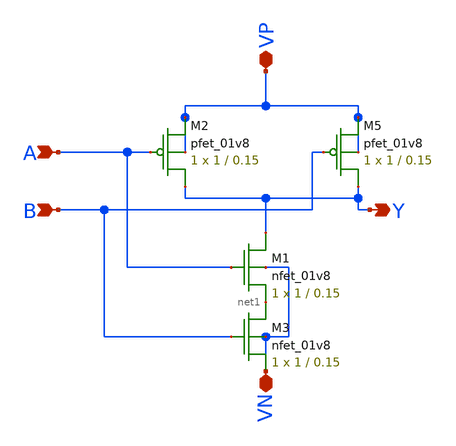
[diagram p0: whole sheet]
** sch_path: schematics/nand2.sch
**.subckt nand2 VP VN A B Y
*.iopin VP
*.iopin VN
*.ipin A
*.ipin B
*.opin Y
XM5 Y B VP VP sky130_fd_pr__pfet_01v8 L=0.15 W=1 nf=1 ad='int((nf+1)/2) * W/nf * 0.29' as='int((nf+2)/2) * W/nf * 0.29'
+ pd='2*int((nf+1)/2) * (W/nf + 0.29)' ps='2*int((nf+2)/2) * (W/nf + 0.29)' nrd='0.29 / W' nrs='0.29 / W'
+ sa=0 sb=0 sd=0 mult=1 m=1
XM2 Y A VP VP sky130_fd_pr__pfet_01v8 L=0.15 W=1 nf=1 ad='int((nf+1)/2) * W/nf * 0.29' as='int((nf+2)/2) * W/nf * 0.29'
+ pd='2*int((nf+1)/2) * (W/nf + 0.29)' ps='2*int((nf+2)/2) * (W/nf + 0.29)' nrd='0.29 / W' nrs='0.29 / W'
+ sa=0 sb=0 sd=0 mult=1 m=1
XM1 Y A net1 VN sky130_fd_pr__nfet_01v8 L=0.15 W=1 nf=1 ad='int((nf+1)/2) * W/nf * 0.29' as='int((nf+2)/2) * W/nf * 0.29'
+ pd='2*int((nf+1)/2) * (W/nf + 0.29)' ps='2*int((nf+2)/2) * (W/nf + 0.29)' nrd='0.29 / W' nrs='0.29 / W'
+ sa=0 sb=0 sd=0 mult=1 m=1
XM3 net1 B VN VN sky130_fd_pr__nfet_01v8 L=0.15 W=1 nf=1 ad='int((nf+1)/2) * W/nf * 0.29' as='int((nf+2)/2) * W/nf * 0.29'
+ pd='2*int((nf+1)/2) * (W/nf + 0.29)' ps='2*int((nf+2)/2) * (W/nf + 0.29)' nrd='0.29 / W' nrs='0.29 / W'
+ sa=0 sb=0 sd=0 mult=1 m=1
**.ends
.end
